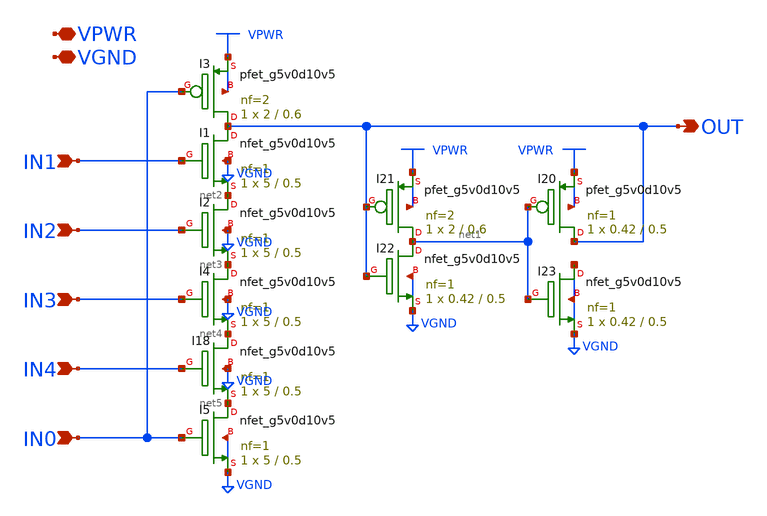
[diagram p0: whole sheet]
** sch_path: gpiov2_amux_nand5.sch
* Copyright 2023 David Mitchell Bailey
* Licensed under the Apache License, Version 2.0 (the "License");
* you may not use this file except in compliance with the License.
* You may obtain a copy of the License at
* https://www.apache.org/licenses/LICENSE-2.0
* Unless required by applicable law or agreed to in writing, software
* distributed under the License is distributed on an "AS IS" BASIS,
* WITHOUT WARRANTIES OR CONDITIONS OF ANY KIND, either express or implied.
* See the License for the specific language governing permissions and
* limitations under the License.
**.subckt gpiov2_amux_nand5 IN1 VPWR VGND IN2 IN0 IN3 OUT IN4
*.ipin IN1
*.iopin VPWR
*.iopin VGND
*.ipin IN2
*.ipin IN0
*.ipin IN3
*.opin OUT
*.ipin IN4
XI1 OUT IN1 net2 VGND sky130_fd_pr__nfet_g5v0d10v5 L=0.5 W=5 nf=1 ad='int((nf+1)/2) * W/nf * 0.29' as='int((nf+2)/2) * W/nf * 0.29'
+ pd='2*int((nf+1)/2) * (W/nf + 0.29)' ps='2*int((nf+2)/2) * (W/nf + 0.29)' nrd='0.29 / W' nrs='0.29 / W'
+ sa=0 sb=0 sd=0 mult=1 m=1
XI3 OUT IN0 VPWR VPWR sky130_fd_pr__pfet_g5v0d10v5 L=0.6 W=2 nf=2 ad='int((nf+1)/2) * W/nf * 0.29' as='int((nf+2)/2) * W/nf * 0.29'
+ pd='2*int((nf+1)/2) * (W/nf + 0.29)' ps='2*int((nf+2)/2) * (W/nf + 0.29)' nrd='0.29 / W' nrs='0.29 / W'
+ sa=0 sb=0 sd=0 mult=1 m=1
XI2 net2 IN2 net3 VGND sky130_fd_pr__nfet_g5v0d10v5 L=0.5 W=5 nf=1 ad='int((nf+1)/2) * W/nf * 0.29' as='int((nf+2)/2) * W/nf * 0.29'
+ pd='2*int((nf+1)/2) * (W/nf + 0.29)' ps='2*int((nf+2)/2) * (W/nf + 0.29)' nrd='0.29 / W' nrs='0.29 / W'
+ sa=0 sb=0 sd=0 mult=1 m=1
XI4 net3 IN3 net4 VGND sky130_fd_pr__nfet_g5v0d10v5 L=0.5 W=5 nf=1 ad='int((nf+1)/2) * W/nf * 0.29' as='int((nf+2)/2) * W/nf * 0.29'
+ pd='2*int((nf+1)/2) * (W/nf + 0.29)' ps='2*int((nf+2)/2) * (W/nf + 0.29)' nrd='0.29 / W' nrs='0.29 / W'
+ sa=0 sb=0 sd=0 mult=1 m=1
XI5 net5 IN0 VGND VGND sky130_fd_pr__nfet_g5v0d10v5 L=0.5 W=5 nf=1 ad='int((nf+1)/2) * W/nf * 0.29' as='int((nf+2)/2) * W/nf * 0.29'
+ pd='2*int((nf+1)/2) * (W/nf + 0.29)' ps='2*int((nf+2)/2) * (W/nf + 0.29)' nrd='0.29 / W' nrs='0.29 / W'
+ sa=0 sb=0 sd=0 mult=1 m=1
XI22 net1 OUT VGND VGND sky130_fd_pr__nfet_g5v0d10v5 L=0.5 W=0.42 nf=1 ad='int((nf+1)/2) * W/nf * 0.29'
+ as='int((nf+2)/2) * W/nf * 0.29' pd='2*int((nf+1)/2) * (W/nf + 0.29)' ps='2*int((nf+2)/2) * (W/nf + 0.29)'
+ nrd='0.29 / W' nrs='0.29 / W' sa=0 sb=0 sd=0 mult=1 m=1
XI21 net1 OUT VPWR VPWR sky130_fd_pr__pfet_g5v0d10v5 L=0.6 W=2 nf=2 ad='int((nf+1)/2) * W/nf * 0.29'
+ as='int((nf+2)/2) * W/nf * 0.29' pd='2*int((nf+1)/2) * (W/nf + 0.29)' ps='2*int((nf+2)/2) * (W/nf + 0.29)'
+ nrd='0.29 / W' nrs='0.29 / W' sa=0 sb=0 sd=0 mult=1 m=1
XI23 VGND net1 VGND VGND sky130_fd_pr__nfet_g5v0d10v5 L=0.5 W=0.42 nf=1 ad='int((nf+1)/2) * W/nf * 0.29'
+ as='int((nf+2)/2) * W/nf * 0.29' pd='2*int((nf+1)/2) * (W/nf + 0.29)' ps='2*int((nf+2)/2) * (W/nf + 0.29)'
+ nrd='0.29 / W' nrs='0.29 / W' sa=0 sb=0 sd=0 mult=1 m=1
XI20 OUT net1 VPWR VPWR sky130_fd_pr__pfet_g5v0d10v5 L=0.5 W=0.42 nf=1 ad='int((nf+1)/2) * W/nf * 0.29'
+ as='int((nf+2)/2) * W/nf * 0.29' pd='2*int((nf+1)/2) * (W/nf + 0.29)' ps='2*int((nf+2)/2) * (W/nf + 0.29)'
+ nrd='0.29 / W' nrs='0.29 / W' sa=0 sb=0 sd=0 mult=1 m=1
XI18 net4 IN4 net5 VGND sky130_fd_pr__nfet_g5v0d10v5 L=0.5 W=5 nf=1 ad='int((nf+1)/2) * W/nf * 0.29'
+ as='int((nf+2)/2) * W/nf * 0.29' pd='2*int((nf+1)/2) * (W/nf + 0.29)' ps='2*int((nf+2)/2) * (W/nf + 0.29)'
+ nrd='0.29 / W' nrs='0.29 / W' sa=0 sb=0 sd=0 mult=1 m=1
**.ends
.end
